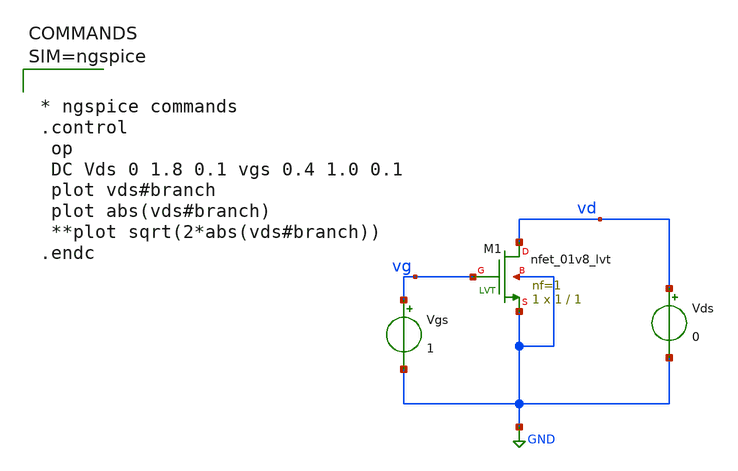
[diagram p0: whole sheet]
** sch_path: xschem/id_vds_nmos.sch
**.subckt id_vds_nmos
XM1 vd vg GND GND sky130_fd_pr__nfet_01v8_lvt L=1 W=1 nf=1 ad='int((1 + 1)/2) * 1 / 1 * 0.29' as='int((1 + 2)/2) * 1 / 1 * 0.29'
+ pd='2*int((1 + 1)/2) * (1 / 1 + 0.29)' ps='2*int((1 + 2)/2) * (1 / 1 + 0.29)' nrd='0.29 / 1 ' nrs='0.29 / 1 '
+ sa=0 sb=0 sd=0 mult=1 m=1
Vgs vg GND 1
Vds vd GND 0
**** begin user architecture code

** opencircuitdesign pdks install
.lib $::SKYWATER_MODELS/sky130.lib.spice tt




* ngspice commands
.control
 op
 DC Vds 0 1.8 0.1 vgs 0.4 1.0 0.1
 plot vds#branch
 plot abs(vds#branch)
 **plot sqrt(2*abs(vds#branch))
.endc



**** end user architecture code
**.ends
.GLOBAL GND
.end
